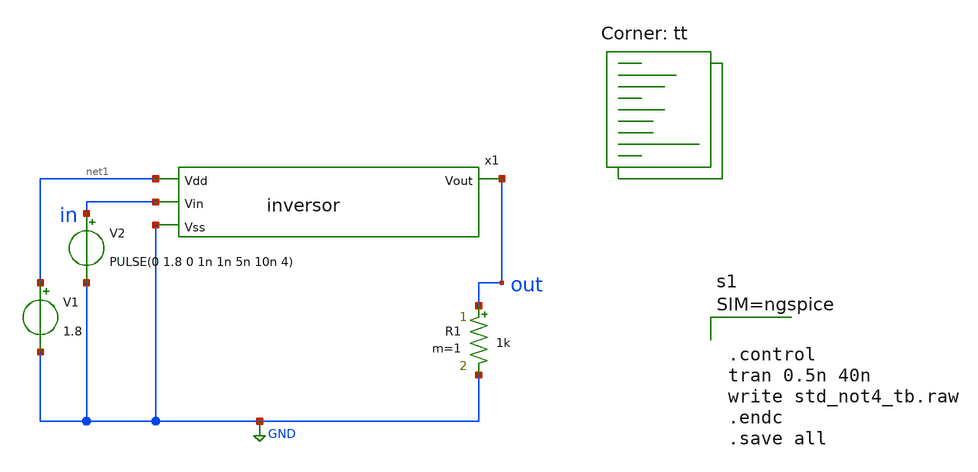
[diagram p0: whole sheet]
** sch_path: tp6/archivos/simulacion.sch
**.subckt simulacion
V1 net1 GND 1.8
V2 in GND PULSE(0 1.8 0 1n 1n 5n 10n 4)
R1 out GND 1k m=1
x1 net1 in out GND inversor
**** begin user architecture code
.lib $::SKYWATER_MODELS/sky130.lib.spice tt



.control
tran 0.5n 40n
write std_not4_tb.raw
.endc
.save all



**** end user architecture code
**.ends

* expanding   symbol:  /home/gaston/Documents/inversor.sym # of pins=4
** sym_path: tp6/archivos/inversor.sym
** sch_path: tp6/archivos/inversor.sch
.subckt inversor Vdd Vin Vout Vss
*.ipin Vdd
*.ipin Vss
*.ipin Vin
*.opin Vout
XM2 Vout Vin Vdd Vdd sky130_fd_pr__pfet_01v8 L=0.15 W=2.1 nf=1 ad='int((nf+1)/2) * W/nf * 0.29' as='int((nf+2)/2) * W/nf * 0.29'
+ pd='2*int((nf+1)/2) * (W/nf + 0.29)' ps='2*int((nf+2)/2) * (W/nf + 0.29)' nrd='0.29 / W' nrs='0.29 / W'
+ sa=0 sb=0 sd=0 mult=1 m=1
XM1 Vout Vin Vss Vss sky130_fd_pr__nfet_01v8 L=0.15 W=1.05 nf=1 ad='int((nf+1)/2) * W/nf * 0.29' as='int((nf+2)/2) * W/nf * 0.29'
+ pd='2*int((nf+1)/2) * (W/nf + 0.29)' ps='2*int((nf+2)/2) * (W/nf + 0.29)' nrd='0.29 / W' nrs='0.29 / W'
+ sa=0 sb=0 sd=0 mult=1 m=1
.ends

.GLOBAL GND
.end
